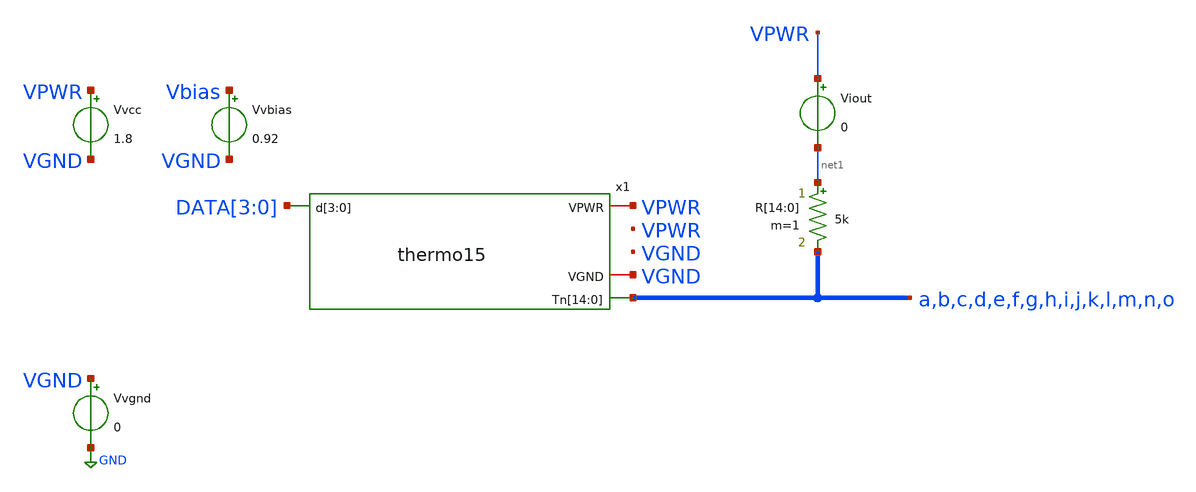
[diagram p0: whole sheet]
** sch_path: xschem/tb_thermo15.sch
**.subckt tb_thermo15
Vvcc VPWR VGND 1.8
R[14] net1 a 5k m=1
R[13] net1 b 5k m=1
R[12] net1 c 5k m=1
R[11] net1 d 5k m=1
R[10] net1 e 5k m=1
R[9] net1 f 5k m=1
R[8] net1 g 5k m=1
R[7] net1 h 5k m=1
R[6] net1 i 5k m=1
R[5] net1 j 5k m=1
R[4] net1 k 5k m=1
R[3] net1 l 5k m=1
R[2] net1 m 5k m=1
R[1] net1 n 5k m=1
R[0] net1 o 5k m=1
Vvbias Vbias VGND 0.92
Vvgnd VGND GND 0
Viout VPWR net1 0
x1 VPWR VGND a b c d e f g h i j k l m n o DATA[3] DATA[2] DATA[1] DATA[0] thermo15
**** begin user architecture code



Vxp0 DATA[0]  GND pulse 1.8v 0v 0n 1n 1n 39n 80n
Vxp1 DATA[1]  GND pulse 1.8v 0v 0n 1n 1n 79n 160n
Vxp2 DATA[2]  GND pulse 1.8v 0v 0n 1n 1n 159n 320n
Vxp3 DATA[3]  GND pulse 1.8v 0v 0n 1n 1n 319n 640n

*.options savecurrents
.control

    save all
    tran 1n 12.8u
    write tb_row15x.raw a b c d e f g h i j k l m n o

.endc




.lib $::SKYWATER_MODELS/sky130.lib.spice tt
.include $::SKYWATER_STDCELLS/sky130_fd_sc_hd.spice

**** end user architecture code
**.ends

* expanding   symbol:  thermo15.sym # of pins=4
** sym_path: xschem/thermo15.sym
** sch_path: xschem/thermo15.sch
.subckt thermo15 VPWR VGND Tn[14] Tn[13] Tn[12] Tn[11] Tn[10] Tn[9] Tn[8] Tn[7] Tn[6] Tn[5] Tn[4]
+ Tn[3] Tn[2] Tn[1] Tn[0] d[3] d[2] d[1] d[0]
*.iopin VPWR
*.ipin d[3],d[2],d[1],d[0]
*.iopin VGND
*.opin
*+ Tn[14],Tn[13],Tn[12],Tn[11],Tn[10],Tn[9],Tn[8],Tn[7],Tn[6],Tn[5],Tn[4],Tn[3],Tn[2],Tn[1],Tn[0]
XTA2 d[1] VGND VGND VPWR VPWR TA2 sky130_fd_sc_hd__inv_1
XTBN TAN2 VGND VGND VPWR VPWR TBN sky130_fd_sc_hd__inv_2
XTA3 d[0] d[1] VGND VGND VPWR VPWR TA3 sky130_fd_sc_hd__nand2_1
XTA1 d[0] d[1] VGND VGND VPWR VPWR TA1 sky130_fd_sc_hd__nor2_1
XTAN d[2] VGND VGND VPWR VPWR TAN sky130_fd_sc_hd__inv_1
XTB1 TA1 TAN VGND VGND VPWR VPWR TB1 sky130_fd_sc_hd__nand2_1
XTB2 TA2 TAN VGND VGND VPWR VPWR TB2 sky130_fd_sc_hd__nand2_1
XTB3 TA3 TAN VGND VGND VPWR VPWR TB3 sky130_fd_sc_hd__nand2_1
XTB4 TAN VGND VGND VPWR VPWR TB4 sky130_fd_sc_hd__inv_1
XTB5 TA1 TAN VGND VGND VPWR VPWR TB5 sky130_fd_sc_hd__nor2_1
XTB6 TA2 TAN VGND VGND VPWR VPWR TB6 sky130_fd_sc_hd__nor2_1
XTB7 TA3 TAN VGND VGND VPWR VPWR TB7 sky130_fd_sc_hd__nor2_1
XOTn0 TB1 TBN VGND VGND VPWR VPWR Tn[0] sky130_fd_sc_hd__nor2_4
XOTn1 TB2 TBN VGND VGND VPWR VPWR Tn[1] sky130_fd_sc_hd__nor2_4
XOTn2 TB3 TBN VGND VGND VPWR VPWR Tn[2] sky130_fd_sc_hd__nor2_4
XOTn3 TB4 TBN VGND VGND VPWR VPWR Tn[3] sky130_fd_sc_hd__nor2_4
XOTn4 TB5 TBN VGND VGND VPWR VPWR Tn[4] sky130_fd_sc_hd__nor2_4
XOTn5 TB6 TBN VGND VGND VPWR VPWR Tn[5] sky130_fd_sc_hd__nor2_4
XOTn6 TB7 TBN VGND VGND VPWR VPWR Tn[6] sky130_fd_sc_hd__nor2_4
XOTn7 TBN VGND VGND VPWR VPWR Tn[7] sky130_fd_sc_hd__inv_4
XOTn8 TB1 TBN VGND VGND VPWR VPWR Tn[8] sky130_fd_sc_hd__nand2_4
XOTn9 TB2 TBN VGND VGND VPWR VPWR Tn[9] sky130_fd_sc_hd__nand2_4
XOTn10 TB3 TBN VGND VGND VPWR VPWR Tn[10] sky130_fd_sc_hd__nand2_4
XOTn11 TB4 TBN VGND VGND VPWR VPWR Tn[11] sky130_fd_sc_hd__nand2_4
XOTn12 TB5 TBN VGND VGND VPWR VPWR Tn[12] sky130_fd_sc_hd__nand2_4
XOTn13 TB6 TBN VGND VGND VPWR VPWR Tn[13] sky130_fd_sc_hd__nand2_4
XOTn14 TB7 TBN VGND VGND VPWR VPWR Tn[14] sky130_fd_sc_hd__nand2_4
XTAN2 d[3] VGND VGND VPWR VPWR TAN2 sky130_fd_sc_hd__inv_1
.ends

.GLOBAL GND
.end
